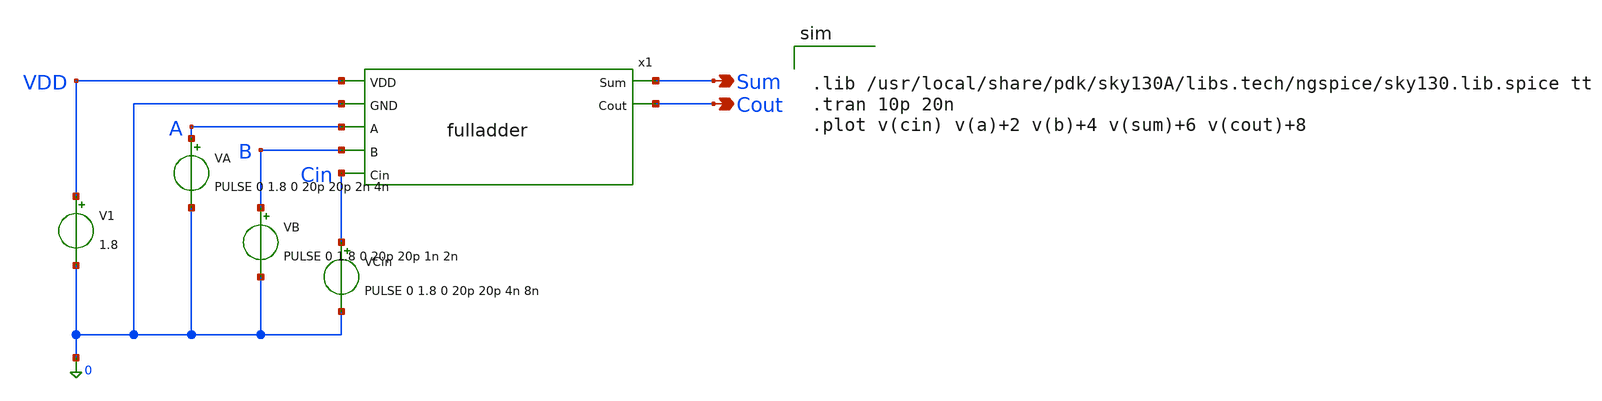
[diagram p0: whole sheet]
** sch_path: testbench/fa_tb_tran.sch
**.subckt fa_tb_tran Sum Cout
*.opin Sum
*.opin Cout
x1 VDD 0 Sum A B Cin Cout fulladder
V1 VDD 0 1.8
VA A 0 PULSE 0 1.8 0 20p 20p 2n 4n
VB B 0 PULSE 0 1.8 0 20p 20p 1n 2n
VCin Cin 0 PULSE 0 1.8 0 20p 20p 4n 8n
**** begin user architecture code


.lib /usr/local/share/pdk/sky130A/libs.tech/ngspice/sky130.lib.spice tt
.tran 10p 20n
.plot v(cin) v(a)+2 v(b)+4 v(sum)+6 v(cout)+8


**** end user architecture code
**.ends
.end
